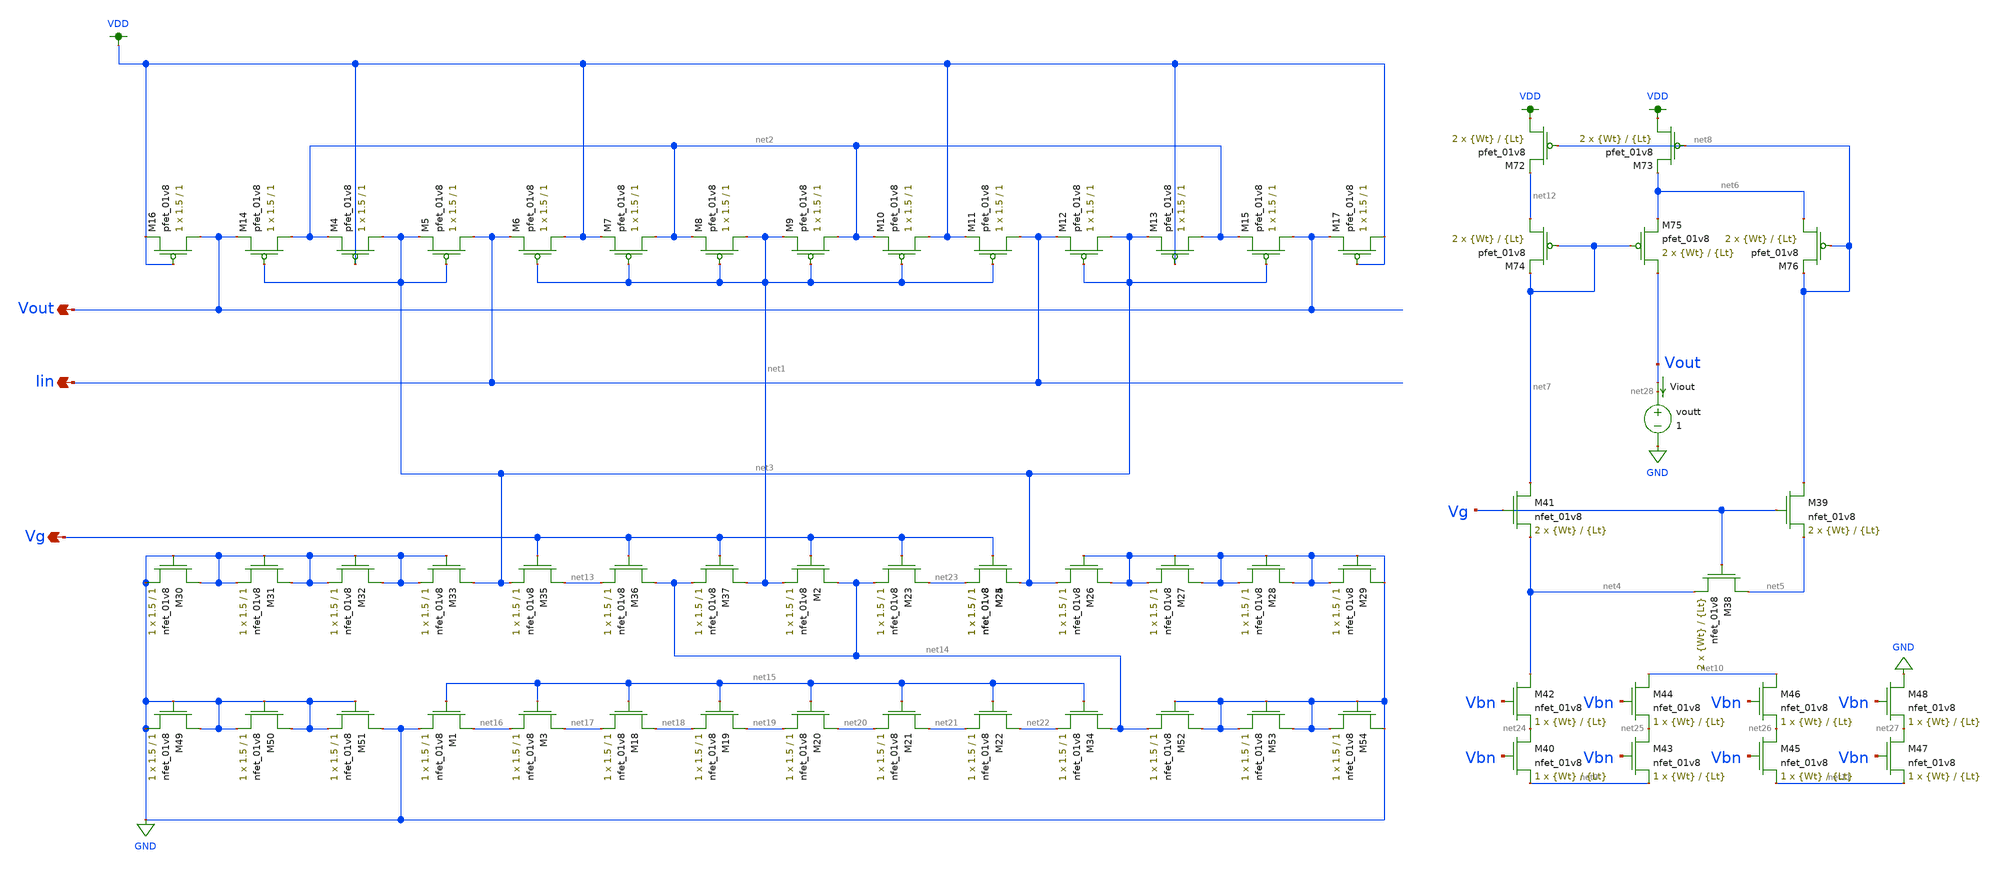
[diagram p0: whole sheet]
** sch_path: schematic/LDS/low-voltage_super-wilson.sch
**.subckt low-voltage_super-wilson Vout Iin Vg
*.opin Vout
*.opin Iin
*.opin Vg
XM4 net3 VDD net2 VDD sky130_fd_pr__pfet_01v8 L=1 W=1.5 nf=1 ad='int((nf+1)/2) * W/nf * 0.29' as='int((nf+2)/2) * W/nf * 0.29'
+ pd='2*int((nf+1)/2) * (W/nf + 0.29)' ps='2*int((nf+2)/2) * (W/nf + 0.29)' nrd='0.29 / W' nrs='0.29 / W'
+ sa=0 sb=0 sd=0 mult=1 m=1
XM5 Iin net3 net3 VDD sky130_fd_pr__pfet_01v8 L=1 W=1.5 nf=1 ad='int((nf+1)/2) * W/nf * 0.29' as='int((nf+2)/2) * W/nf * 0.29'
+ pd='2*int((nf+1)/2) * (W/nf + 0.29)' ps='2*int((nf+2)/2) * (W/nf + 0.29)' nrd='0.29 / W' nrs='0.29 / W'
+ sa=0 sb=0 sd=0 mult=1 m=1
XM6 VDD net1 Iin VDD sky130_fd_pr__pfet_01v8 L=1 W=1.5 nf=1 ad='int((nf+1)/2) * W/nf * 0.29' as='int((nf+2)/2) * W/nf * 0.29'
+ pd='2*int((nf+1)/2) * (W/nf + 0.29)' ps='2*int((nf+2)/2) * (W/nf + 0.29)' nrd='0.29 / W' nrs='0.29 / W'
+ sa=0 sb=0 sd=0 mult=1 m=1
XM7 net2 net1 VDD VDD sky130_fd_pr__pfet_01v8 L=1 W=1.5 nf=1 ad='int((nf+1)/2) * W/nf * 0.29' as='int((nf+2)/2) * W/nf * 0.29'
+ pd='2*int((nf+1)/2) * (W/nf + 0.29)' ps='2*int((nf+2)/2) * (W/nf + 0.29)' nrd='0.29 / W' nrs='0.29 / W'
+ sa=0 sb=0 sd=0 mult=1 m=1
XM8 net1 net1 net2 VDD sky130_fd_pr__pfet_01v8 L=1 W=1.5 nf=1 ad='int((nf+1)/2) * W/nf * 0.29' as='int((nf+2)/2) * W/nf * 0.29'
+ pd='2*int((nf+1)/2) * (W/nf + 0.29)' ps='2*int((nf+2)/2) * (W/nf + 0.29)' nrd='0.29 / W' nrs='0.29 / W'
+ sa=0 sb=0 sd=0 mult=1 m=1
XM9 net2 net1 net1 VDD sky130_fd_pr__pfet_01v8 L=1 W=1.5 nf=1 ad='int((nf+1)/2) * W/nf * 0.29' as='int((nf+2)/2) * W/nf * 0.29'
+ pd='2*int((nf+1)/2) * (W/nf + 0.29)' ps='2*int((nf+2)/2) * (W/nf + 0.29)' nrd='0.29 / W' nrs='0.29 / W'
+ sa=0 sb=0 sd=0 mult=1 m=1
XM10 VDD net1 net2 VDD sky130_fd_pr__pfet_01v8 L=1 W=1.5 nf=1 ad='int((nf+1)/2) * W/nf * 0.29' as='int((nf+2)/2) * W/nf * 0.29'
+ pd='2*int((nf+1)/2) * (W/nf + 0.29)' ps='2*int((nf+2)/2) * (W/nf + 0.29)' nrd='0.29 / W' nrs='0.29 / W'
+ sa=0 sb=0 sd=0 mult=1 m=1
XM11 Iin net1 VDD VDD sky130_fd_pr__pfet_01v8 L=1 W=1.5 nf=1 ad='int((nf+1)/2) * W/nf * 0.29' as='int((nf+2)/2) * W/nf * 0.29'
+ pd='2*int((nf+1)/2) * (W/nf + 0.29)' ps='2*int((nf+2)/2) * (W/nf + 0.29)' nrd='0.29 / W' nrs='0.29 / W'
+ sa=0 sb=0 sd=0 mult=1 m=1
XM12 net3 net3 Iin VDD sky130_fd_pr__pfet_01v8 L=1 W=1.5 nf=1 ad='int((nf+1)/2) * W/nf * 0.29' as='int((nf+2)/2) * W/nf * 0.29'
+ pd='2*int((nf+1)/2) * (W/nf + 0.29)' ps='2*int((nf+2)/2) * (W/nf + 0.29)' nrd='0.29 / W' nrs='0.29 / W'
+ sa=0 sb=0 sd=0 mult=1 m=1
XM13 net2 VDD net3 VDD sky130_fd_pr__pfet_01v8 L=1 W=1.5 nf=1 ad='int((nf+1)/2) * W/nf * 0.29' as='int((nf+2)/2) * W/nf * 0.29'
+ pd='2*int((nf+1)/2) * (W/nf + 0.29)' ps='2*int((nf+2)/2) * (W/nf + 0.29)' nrd='0.29 / W' nrs='0.29 / W'
+ sa=0 sb=0 sd=0 mult=1 m=1
XM14 net2 net3 Vout VDD sky130_fd_pr__pfet_01v8 L=1 W=1.5 nf=1 ad='int((nf+1)/2) * W/nf * 0.29' as='int((nf+2)/2) * W/nf * 0.29'
+ pd='2*int((nf+1)/2) * (W/nf + 0.29)' ps='2*int((nf+2)/2) * (W/nf + 0.29)' nrd='0.29 / W' nrs='0.29 / W'
+ sa=0 sb=0 sd=0 mult=1 m=1
XM15 Vout net3 net2 VDD sky130_fd_pr__pfet_01v8 L=1 W=1.5 nf=1 ad='int((nf+1)/2) * W/nf * 0.29' as='int((nf+2)/2) * W/nf * 0.29'
+ pd='2*int((nf+1)/2) * (W/nf + 0.29)' ps='2*int((nf+2)/2) * (W/nf + 0.29)' nrd='0.29 / W' nrs='0.29 / W'
+ sa=0 sb=0 sd=0 mult=1 m=1
XM16 Vout VDD VDD VDD sky130_fd_pr__pfet_01v8 L=1 W=1.5 nf=1 ad='int((nf+1)/2) * W/nf * 0.29' as='int((nf+2)/2) * W/nf * 0.29'
+ pd='2*int((nf+1)/2) * (W/nf + 0.29)' ps='2*int((nf+2)/2) * (W/nf + 0.29)' nrd='0.29 / W' nrs='0.29 / W'
+ sa=0 sb=0 sd=0 mult=1 m=1
XM17 VDD VDD Vout VDD sky130_fd_pr__pfet_01v8 L=1 W=1.5 nf=1 ad='int((nf+1)/2) * W/nf * 0.29' as='int((nf+2)/2) * W/nf * 0.29'
+ pd='2*int((nf+1)/2) * (W/nf + 0.29)' ps='2*int((nf+2)/2) * (W/nf + 0.29)' nrd='0.29 / W' nrs='0.29 / W'
+ sa=0 sb=0 sd=0 mult=1 m=1
XM1 net16 net15 GND GND sky130_fd_pr__nfet_01v8 L=1 W=1.5 nf=1 ad='int((nf+1)/2) * W/nf * 0.29' as='int((nf+2)/2) * W/nf * 0.29'
+ pd='2*int((nf+1)/2) * (W/nf + 0.29)' ps='2*int((nf+2)/2) * (W/nf + 0.29)' nrd='0.29 / W' nrs='0.29 / W'
+ sa=0 sb=0 sd=0 mult=1 m=1
XM3 net17 net15 net16 GND sky130_fd_pr__nfet_01v8 L=1 W=1.5 nf=1 ad='int((nf+1)/2) * W/nf * 0.29' as='int((nf+2)/2) * W/nf * 0.29'
+ pd='2*int((nf+1)/2) * (W/nf + 0.29)' ps='2*int((nf+2)/2) * (W/nf + 0.29)' nrd='0.29 / W' nrs='0.29 / W'
+ sa=0 sb=0 sd=0 mult=1 m=1
XM18 net18 net15 net17 GND sky130_fd_pr__nfet_01v8 L=1 W=1.5 nf=1 ad='int((nf+1)/2) * W/nf * 0.29' as='int((nf+2)/2) * W/nf * 0.29'
+ pd='2*int((nf+1)/2) * (W/nf + 0.29)' ps='2*int((nf+2)/2) * (W/nf + 0.29)' nrd='0.29 / W' nrs='0.29 / W'
+ sa=0 sb=0 sd=0 mult=1 m=1
XM19 net19 net15 net18 GND sky130_fd_pr__nfet_01v8 L=1 W=1.5 nf=1 ad='int((nf+1)/2) * W/nf * 0.29' as='int((nf+2)/2) * W/nf * 0.29'
+ pd='2*int((nf+1)/2) * (W/nf + 0.29)' ps='2*int((nf+2)/2) * (W/nf + 0.29)' nrd='0.29 / W' nrs='0.29 / W'
+ sa=0 sb=0 sd=0 mult=1 m=1
XM20 net20 net15 net19 GND sky130_fd_pr__nfet_01v8 L=1 W=1.5 nf=1 ad='int((nf+1)/2) * W/nf * 0.29' as='int((nf+2)/2) * W/nf * 0.29'
+ pd='2*int((nf+1)/2) * (W/nf + 0.29)' ps='2*int((nf+2)/2) * (W/nf + 0.29)' nrd='0.29 / W' nrs='0.29 / W'
+ sa=0 sb=0 sd=0 mult=1 m=1
XM21 net21 net15 net20 GND sky130_fd_pr__nfet_01v8 L=1 W=1.5 nf=1 ad='int((nf+1)/2) * W/nf * 0.29' as='int((nf+2)/2) * W/nf * 0.29'
+ pd='2*int((nf+1)/2) * (W/nf + 0.29)' ps='2*int((nf+2)/2) * (W/nf + 0.29)' nrd='0.29 / W' nrs='0.29 / W'
+ sa=0 sb=0 sd=0 mult=1 m=1
XM22 net22 net15 net21 GND sky130_fd_pr__nfet_01v8 L=1 W=1.5 nf=1 ad='int((nf+1)/2) * W/nf * 0.29' as='int((nf+2)/2) * W/nf * 0.29'
+ pd='2*int((nf+1)/2) * (W/nf + 0.29)' ps='2*int((nf+2)/2) * (W/nf + 0.29)' nrd='0.29 / W' nrs='0.29 / W'
+ sa=0 sb=0 sd=0 mult=1 m=1
XM34 net14 net15 net22 GND sky130_fd_pr__nfet_01v8 L=1 W=1.5 nf=1 ad='int((nf+1)/2) * W/nf * 0.29' as='int((nf+2)/2) * W/nf * 0.29'
+ pd='2*int((nf+1)/2) * (W/nf + 0.29)' ps='2*int((nf+2)/2) * (W/nf + 0.29)' nrd='0.29 / W' nrs='0.29 / W'
+ sa=0 sb=0 sd=0 mult=1 m=1
XM35 net13 Vg net3 GND sky130_fd_pr__nfet_01v8 L=1 W=1.5 nf=1 ad='int((nf+1)/2) * W/nf * 0.29' as='int((nf+2)/2) * W/nf * 0.29'
+ pd='2*int((nf+1)/2) * (W/nf + 0.29)' ps='2*int((nf+2)/2) * (W/nf + 0.29)' nrd='0.29 / W' nrs='0.29 / W'
+ sa=0 sb=0 sd=0 mult=1 m=1
XM36 net14 Vg net13 GND sky130_fd_pr__nfet_01v8 L=1 W=1.5 nf=1 ad='int((nf+1)/2) * W/nf * 0.29' as='int((nf+2)/2) * W/nf * 0.29'
+ pd='2*int((nf+1)/2) * (W/nf + 0.29)' ps='2*int((nf+2)/2) * (W/nf + 0.29)' nrd='0.29 / W' nrs='0.29 / W'
+ sa=0 sb=0 sd=0 mult=1 m=1
XM37 net1 Vg net14 GND sky130_fd_pr__nfet_01v8 L=1 W=1.5 nf=1 ad='int((nf+1)/2) * W/nf * 0.29' as='int((nf+2)/2) * W/nf * 0.29'
+ pd='2*int((nf+1)/2) * (W/nf + 0.29)' ps='2*int((nf+2)/2) * (W/nf + 0.29)' nrd='0.29 / W' nrs='0.29 / W'
+ sa=0 sb=0 sd=0 mult=1 m=1
XM38 net5 Vg net4 GND sky130_fd_pr__nfet_01v8 L={Lt} W={Wt} nf=1 ad='int((nf+1)/2) * W/nf * 0.29' as='int((nf+2)/2) * W/nf * 0.29'
+ pd='2*int((nf+1)/2) * (W/nf + 0.29)' ps='2*int((nf+2)/2) * (W/nf + 0.29)' nrd='0.29 / W' nrs='0.29 / W'
+ sa=0 sb=0 sd=0 mult=2 m=2
XM39 net8 Vg net5 GND sky130_fd_pr__nfet_01v8 L={Lt} W={Wt} nf=1 ad='int((nf+1)/2) * W/nf * 0.29' as='int((nf+2)/2) * W/nf * 0.29'
+ pd='2*int((nf+1)/2) * (W/nf + 0.29)' ps='2*int((nf+2)/2) * (W/nf + 0.29)' nrd='0.29 / W' nrs='0.29 / W'
+ sa=0 sb=0 sd=0 mult=2 m=2
XM40 net24 Vbn net9 GND sky130_fd_pr__nfet_01v8 L={Lt} W={Wt} nf=1 ad='int((nf+1)/2) * W/nf * 0.29' as='int((nf+2)/2) * W/nf * 0.29'
+ pd='2*int((nf+1)/2) * (W/nf + 0.29)' ps='2*int((nf+2)/2) * (W/nf + 0.29)' nrd='0.29 / W' nrs='0.29 / W'
+ sa=0 sb=0 sd=0 mult=1 m=1
XM41 net7 Vg net4 GND sky130_fd_pr__nfet_01v8 L={Lt} W={Wt} nf=1 ad='int((nf+1)/2) * W/nf * 0.29' as='int((nf+2)/2) * W/nf * 0.29'
+ pd='2*int((nf+1)/2) * (W/nf + 0.29)' ps='2*int((nf+2)/2) * (W/nf + 0.29)' nrd='0.29 / W' nrs='0.29 / W'
+ sa=0 sb=0 sd=0 mult=2 m=2
XM72 VDD net8 net12 VDD sky130_fd_pr__pfet_01v8 L={Lt} W={Wt} nf=1 ad='int((nf+1)/2) * W/nf * 0.29' as='int((nf+2)/2) * W/nf * 0.29'
+ pd='2*int((nf+1)/2) * (W/nf + 0.29)' ps='2*int((nf+2)/2) * (W/nf + 0.29)' nrd='0.29 / W' nrs='0.29 / W'
+ sa=0 sb=0 sd=0 mult=2 m=2
XM73 VDD net8 net6 VDD sky130_fd_pr__pfet_01v8 L={Lt} W={Wt} nf=1 ad='int((nf+1)/2) * W/nf * 0.29' as='int((nf+2)/2) * W/nf * 0.29'
+ pd='2*int((nf+1)/2) * (W/nf + 0.29)' ps='2*int((nf+2)/2) * (W/nf + 0.29)' nrd='0.29 / W' nrs='0.29 / W'
+ sa=0 sb=0 sd=0 mult=2 m=2
XM74 net12 net7 net7 VDD sky130_fd_pr__pfet_01v8 L={Lt} W={Wt} nf=1 ad='int((nf+1)/2) * W/nf * 0.29'
+ as='int((nf+2)/2) * W/nf * 0.29' pd='2*int((nf+1)/2) * (W/nf + 0.29)' ps='2*int((nf+2)/2) * (W/nf + 0.29)'
+ nrd='0.29 / W' nrs='0.29 / W' sa=0 sb=0 sd=0 mult=2 m=2
XM75 Vout net7 net6 VDD sky130_fd_pr__pfet_01v8 L={Lt} W={Wt} nf=1 ad='int((nf+1)/2) * W/nf * 0.29' as='int((nf+2)/2) * W/nf * 0.29'
+ pd='2*int((nf+1)/2) * (W/nf + 0.29)' ps='2*int((nf+2)/2) * (W/nf + 0.29)' nrd='0.29 / W' nrs='0.29 / W'
+ sa=0 sb=0 sd=0 mult=2 m=2
XM76 net6 net8 net8 VDD sky130_fd_pr__pfet_01v8 L={Lt} W={Wt} nf=1 ad='int((nf+1)/2) * W/nf * 0.29' as='int((nf+2)/2) * W/nf * 0.29'
+ pd='2*int((nf+1)/2) * (W/nf + 0.29)' ps='2*int((nf+2)/2) * (W/nf + 0.29)' nrd='0.29 / W' nrs='0.29 / W'
+ sa=0 sb=0 sd=0 mult=2 m=2
XM42 net4 Vbn net24 GND sky130_fd_pr__nfet_01v8 L={Lt} W={Wt} nf=1 ad='int((nf+1)/2) * W/nf * 0.29' as='int((nf+2)/2) * W/nf * 0.29'
+ pd='2*int((nf+1)/2) * (W/nf + 0.29)' ps='2*int((nf+2)/2) * (W/nf + 0.29)' nrd='0.29 / W' nrs='0.29 / W'
+ sa=0 sb=0 sd=0 mult=1 m=1
XM43 net25 Vbn net9 GND sky130_fd_pr__nfet_01v8 L={Lt} W={Wt} nf=1 ad='int((nf+1)/2) * W/nf * 0.29' as='int((nf+2)/2) * W/nf * 0.29'
+ pd='2*int((nf+1)/2) * (W/nf + 0.29)' ps='2*int((nf+2)/2) * (W/nf + 0.29)' nrd='0.29 / W' nrs='0.29 / W'
+ sa=0 sb=0 sd=0 mult=1 m=1
XM44 net10 Vbn net25 GND sky130_fd_pr__nfet_01v8 L={Lt} W={Wt} nf=1 ad='int((nf+1)/2) * W/nf * 0.29'
+ as='int((nf+2)/2) * W/nf * 0.29' pd='2*int((nf+1)/2) * (W/nf + 0.29)' ps='2*int((nf+2)/2) * (W/nf + 0.29)'
+ nrd='0.29 / W' nrs='0.29 / W' sa=0 sb=0 sd=0 mult=1 m=1
XM45 net26 Vbn net11 GND sky130_fd_pr__nfet_01v8 L={Lt} W={Wt} nf=1 ad='int((nf+1)/2) * W/nf * 0.29'
+ as='int((nf+2)/2) * W/nf * 0.29' pd='2*int((nf+1)/2) * (W/nf + 0.29)' ps='2*int((nf+2)/2) * (W/nf + 0.29)'
+ nrd='0.29 / W' nrs='0.29 / W' sa=0 sb=0 sd=0 mult=1 m=1
XM46 net10 Vbn net26 GND sky130_fd_pr__nfet_01v8 L={Lt} W={Wt} nf=1 ad='int((nf+1)/2) * W/nf * 0.29'
+ as='int((nf+2)/2) * W/nf * 0.29' pd='2*int((nf+1)/2) * (W/nf + 0.29)' ps='2*int((nf+2)/2) * (W/nf + 0.29)'
+ nrd='0.29 / W' nrs='0.29 / W' sa=0 sb=0 sd=0 mult=1 m=1
XM47 net27 Vbn net11 GND sky130_fd_pr__nfet_01v8 L={Lt} W={Wt} nf=1 ad='int((nf+1)/2) * W/nf * 0.29'
+ as='int((nf+2)/2) * W/nf * 0.29' pd='2*int((nf+1)/2) * (W/nf + 0.29)' ps='2*int((nf+2)/2) * (W/nf + 0.29)'
+ nrd='0.29 / W' nrs='0.29 / W' sa=0 sb=0 sd=0 mult=1 m=1
XM48 GND Vbn net27 GND sky130_fd_pr__nfet_01v8 L={Lt} W={Wt} nf=1 ad='int((nf+1)/2) * W/nf * 0.29' as='int((nf+2)/2) * W/nf * 0.29'
+ pd='2*int((nf+1)/2) * (W/nf + 0.29)' ps='2*int((nf+2)/2) * (W/nf + 0.29)' nrd='0.29 / W' nrs='0.29 / W'
+ sa=0 sb=0 sd=0 mult=1 m=1
voutt net28 GND 1
Viout Vout net28 0
.save i(viout)
XM2 net14 Vg net1 GND sky130_fd_pr__nfet_01v8 L=1 W=1.5 nf=1 ad='int((nf+1)/2) * W/nf * 0.29' as='int((nf+2)/2) * W/nf * 0.29'
+ pd='2*int((nf+1)/2) * (W/nf + 0.29)' ps='2*int((nf+2)/2) * (W/nf + 0.29)' nrd='0.29 / W' nrs='0.29 / W'
+ sa=0 sb=0 sd=0 mult=1 m=1
XM23 net23 Vg net14 GND sky130_fd_pr__nfet_01v8 L=1 W=1.5 nf=1 ad='int((nf+1)/2) * W/nf * 0.29' as='int((nf+2)/2) * W/nf * 0.29'
+ pd='2*int((nf+1)/2) * (W/nf + 0.29)' ps='2*int((nf+2)/2) * (W/nf + 0.29)' nrd='0.29 / W' nrs='0.29 / W'
+ sa=0 sb=0 sd=0 mult=1 m=1
XM24 net3 Vg net23 GND sky130_fd_pr__nfet_01v8 L=1 W=1.5 nf=1 ad='int((nf+1)/2) * W/nf * 0.29' as='int((nf+2)/2) * W/nf * 0.29'
+ pd='2*int((nf+1)/2) * (W/nf + 0.29)' ps='2*int((nf+2)/2) * (W/nf + 0.29)' nrd='0.29 / W' nrs='0.29 / W'
+ sa=0 sb=0 sd=0 mult=1 m=1
XM25 net3 Vg net23 GND sky130_fd_pr__nfet_01v8 L=1 W=1.5 nf=1 ad='int((nf+1)/2) * W/nf * 0.29' as='int((nf+2)/2) * W/nf * 0.29'
+ pd='2*int((nf+1)/2) * (W/nf + 0.29)' ps='2*int((nf+2)/2) * (W/nf + 0.29)' nrd='0.29 / W' nrs='0.29 / W'
+ sa=0 sb=0 sd=0 mult=1 m=1
XM26 GND GND net3 GND sky130_fd_pr__nfet_01v8 L=1 W=1.5 nf=1 ad='int((nf+1)/2) * W/nf * 0.29' as='int((nf+2)/2) * W/nf * 0.29'
+ pd='2*int((nf+1)/2) * (W/nf + 0.29)' ps='2*int((nf+2)/2) * (W/nf + 0.29)' nrd='0.29 / W' nrs='0.29 / W'
+ sa=0 sb=0 sd=0 mult=1 m=1
XM27 GND GND GND GND sky130_fd_pr__nfet_01v8 L=1 W=1.5 nf=1 ad='int((nf+1)/2) * W/nf * 0.29' as='int((nf+2)/2) * W/nf * 0.29'
+ pd='2*int((nf+1)/2) * (W/nf + 0.29)' ps='2*int((nf+2)/2) * (W/nf + 0.29)' nrd='0.29 / W' nrs='0.29 / W'
+ sa=0 sb=0 sd=0 mult=1 m=1
XM28 GND GND GND GND sky130_fd_pr__nfet_01v8 L=1 W=1.5 nf=1 ad='int((nf+1)/2) * W/nf * 0.29' as='int((nf+2)/2) * W/nf * 0.29'
+ pd='2*int((nf+1)/2) * (W/nf + 0.29)' ps='2*int((nf+2)/2) * (W/nf + 0.29)' nrd='0.29 / W' nrs='0.29 / W'
+ sa=0 sb=0 sd=0 mult=1 m=1
XM29 GND GND GND GND sky130_fd_pr__nfet_01v8 L=1 W=1.5 nf=1 ad='int((nf+1)/2) * W/nf * 0.29' as='int((nf+2)/2) * W/nf * 0.29'
+ pd='2*int((nf+1)/2) * (W/nf + 0.29)' ps='2*int((nf+2)/2) * (W/nf + 0.29)' nrd='0.29 / W' nrs='0.29 / W'
+ sa=0 sb=0 sd=0 mult=1 m=1
XM30 GND GND GND GND sky130_fd_pr__nfet_01v8 L=1 W=1.5 nf=1 ad='int((nf+1)/2) * W/nf * 0.29' as='int((nf+2)/2) * W/nf * 0.29'
+ pd='2*int((nf+1)/2) * (W/nf + 0.29)' ps='2*int((nf+2)/2) * (W/nf + 0.29)' nrd='0.29 / W' nrs='0.29 / W'
+ sa=0 sb=0 sd=0 mult=1 m=1
XM31 GND GND GND GND sky130_fd_pr__nfet_01v8 L=1 W=1.5 nf=1 ad='int((nf+1)/2) * W/nf * 0.29' as='int((nf+2)/2) * W/nf * 0.29'
+ pd='2*int((nf+1)/2) * (W/nf + 0.29)' ps='2*int((nf+2)/2) * (W/nf + 0.29)' nrd='0.29 / W' nrs='0.29 / W'
+ sa=0 sb=0 sd=0 mult=1 m=1
XM32 GND GND GND GND sky130_fd_pr__nfet_01v8 L=1 W=1.5 nf=1 ad='int((nf+1)/2) * W/nf * 0.29' as='int((nf+2)/2) * W/nf * 0.29'
+ pd='2*int((nf+1)/2) * (W/nf + 0.29)' ps='2*int((nf+2)/2) * (W/nf + 0.29)' nrd='0.29 / W' nrs='0.29 / W'
+ sa=0 sb=0 sd=0 mult=1 m=1
XM33 net3 GND GND GND sky130_fd_pr__nfet_01v8 L=1 W=1.5 nf=1 ad='int((nf+1)/2) * W/nf * 0.29' as='int((nf+2)/2) * W/nf * 0.29'
+ pd='2*int((nf+1)/2) * (W/nf + 0.29)' ps='2*int((nf+2)/2) * (W/nf + 0.29)' nrd='0.29 / W' nrs='0.29 / W'
+ sa=0 sb=0 sd=0 mult=1 m=1
XM49 GND GND GND GND sky130_fd_pr__nfet_01v8 L=1 W=1.5 nf=1 ad='int((nf+1)/2) * W/nf * 0.29' as='int((nf+2)/2) * W/nf * 0.29'
+ pd='2*int((nf+1)/2) * (W/nf + 0.29)' ps='2*int((nf+2)/2) * (W/nf + 0.29)' nrd='0.29 / W' nrs='0.29 / W'
+ sa=0 sb=0 sd=0 mult=1 m=1
XM50 GND GND GND GND sky130_fd_pr__nfet_01v8 L=1 W=1.5 nf=1 ad='int((nf+1)/2) * W/nf * 0.29' as='int((nf+2)/2) * W/nf * 0.29'
+ pd='2*int((nf+1)/2) * (W/nf + 0.29)' ps='2*int((nf+2)/2) * (W/nf + 0.29)' nrd='0.29 / W' nrs='0.29 / W'
+ sa=0 sb=0 sd=0 mult=1 m=1
XM51 GND GND GND GND sky130_fd_pr__nfet_01v8 L=1 W=1.5 nf=1 ad='int((nf+1)/2) * W/nf * 0.29' as='int((nf+2)/2) * W/nf * 0.29'
+ pd='2*int((nf+1)/2) * (W/nf + 0.29)' ps='2*int((nf+2)/2) * (W/nf + 0.29)' nrd='0.29 / W' nrs='0.29 / W'
+ sa=0 sb=0 sd=0 mult=1 m=1
XM52 GND GND net14 GND sky130_fd_pr__nfet_01v8 L=1 W=1.5 nf=1 ad='int((nf+1)/2) * W/nf * 0.29' as='int((nf+2)/2) * W/nf * 0.29'
+ pd='2*int((nf+1)/2) * (W/nf + 0.29)' ps='2*int((nf+2)/2) * (W/nf + 0.29)' nrd='0.29 / W' nrs='0.29 / W'
+ sa=0 sb=0 sd=0 mult=1 m=1
XM53 GND GND GND GND sky130_fd_pr__nfet_01v8 L=1 W=1.5 nf=1 ad='int((nf+1)/2) * W/nf * 0.29' as='int((nf+2)/2) * W/nf * 0.29'
+ pd='2*int((nf+1)/2) * (W/nf + 0.29)' ps='2*int((nf+2)/2) * (W/nf + 0.29)' nrd='0.29 / W' nrs='0.29 / W'
+ sa=0 sb=0 sd=0 mult=1 m=1
XM54 GND GND GND GND sky130_fd_pr__nfet_01v8 L=1 W=1.5 nf=1 ad='int((nf+1)/2) * W/nf * 0.29' as='int((nf+2)/2) * W/nf * 0.29'
+ pd='2*int((nf+1)/2) * (W/nf + 0.29)' ps='2*int((nf+2)/2) * (W/nf + 0.29)' nrd='0.29 / W' nrs='0.29 / W'
+ sa=0 sb=0 sd=0 mult=1 m=1
**.ends
.GLOBAL VDD
.GLOBAL GND
.end
